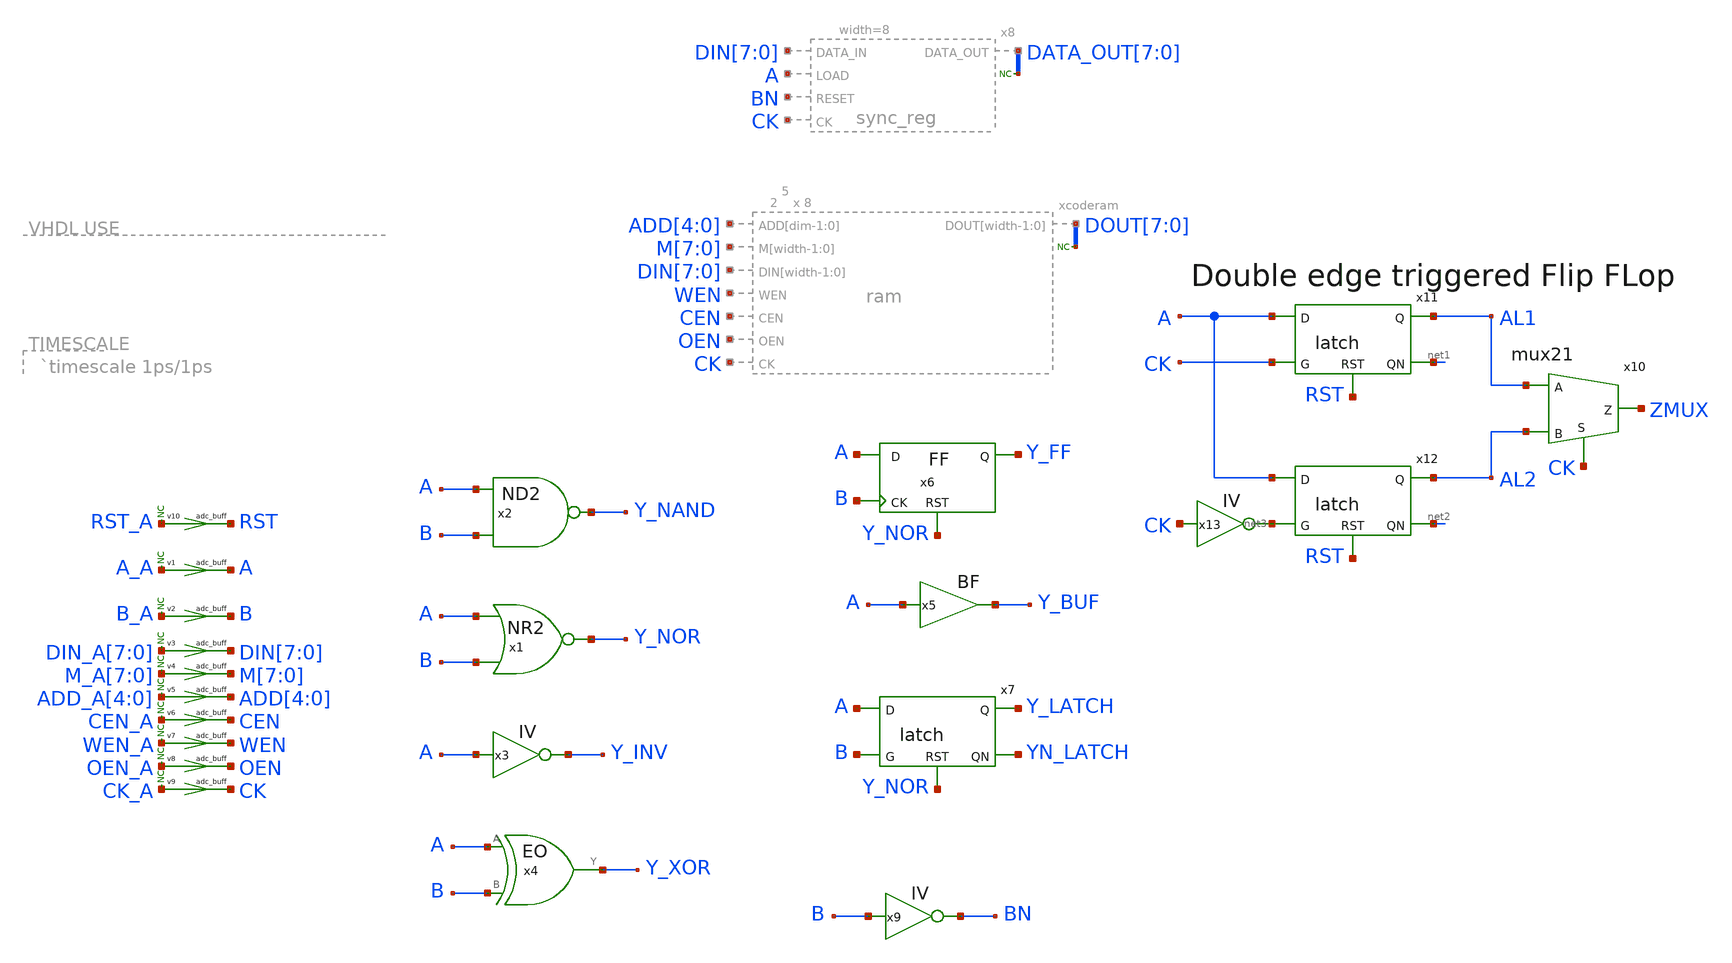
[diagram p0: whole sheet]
** sch_path: xschem_library/logic/testbench.sch
* Copyright (C) 1998-2026 Stefan Frederik Schippers
* This program is free software; you can redistribute it and/or modify
* it under the terms of the GNU General Public License as published by
* the Free Software Foundation; either version 2 of the License, or
* (at your option) any later version.
* This program is distributed in the hope that it will be useful,
* but WITHOUT ANY WARRANTY; without even the implied warranty of
* MERCHANTABILITY or FITNESS FOR A PARTICULAR PURPOSE.  See the
* GNU General Public License for more details.
* You should have received a copy of the GNU General Public License
* along with this program; if not, write to the Free Software
* xschem_library/logic/bf.sym:
* Copyright (C) 1998-2023 Stefan Frederik Schippers
**.subckt testbench
x1 [ A B ] Y_NOR nor
x2 [ A B ] Y_NAND nand
x3 [ A ] Y_INV inv
x4 Y_XOR A B eo
x5 Y_BUF A bf
x6 A Y_FF B Y_NOR ff
x7 A Y_LATCH B Y_NOR YN_LATCH latch
x9 [ B ] BN inv
v1 [ A_A ] [ A ] adc_buff
v2 [ B_A ] [ B ] adc_buff
v3 [ DIN_A[7] ] [ DIN[7] ] adc_buff
v4 [ M_A[7] ] [ M[7] ] adc_buff
v5 [ ADD_A[4] ] [ ADD[4] ] adc_buff
v6 [ CEN_A ] [ CEN ] adc_buff
v7 [ WEN_A ] [ WEN ] adc_buff
v8 [ OEN_A ] [ OEN ] adc_buff
v9 [ CK_A ] [ CK ] adc_buff
x10 AL1 ZMUX AL2 CK mux21
x11 A AL1 CK RST net1 latch
x12 A AL2 net3 RST net2 latch
x13 [ CK ] net3 inv
v10 [ RST_A ] [ RST ] adc_buff
* noconn RST_A
* noconn A_A
* noconn B_A
* noconn DIN_A[7:0]
* noconn M_A[7:0]
* noconn ADD_A[4:0]
* noconn CEN_A
* noconn WEN_A
* noconn OEN_A
* noconn CK_A
* noconn DOUT[7:0]
* noconn DATA_OUT[7:0]
**.ends

* expanding   symbol:  eo.sym # of pins=3
** sym_path: xschem_library/logic/eo.sym
** sch_path: xschem_library/logic/eo.sch
.subckt eo Y A B  delay=220 ps del=220
*.ipin A
*.ipin B
*.opin Y
* noconn Y
* noconn B
* noconn A
.ends


* expanding   symbol:  bf.sym # of pins=2
** sym_path: xschem_library/logic/bf.sym
** sch_path: xschem_library/logic/bf.sch
.subckt bf Y A  delay=90 ps del=90
*.opin Y
*.ipin A
* noconn Y
* noconn A
.ends


* expanding   symbol:  ff.sym # of pins=4
** sym_path: xschem_library/logic/ff.sym
** sch_path: xschem_library/logic/ff.sch
.subckt ff D Q CK RST  delay=400 ps del=400
*.ipin D
*.opin Q
*.ipin CK
*.ipin RST
* noconn Q
* noconn D
* noconn CK
* noconn RST
.ends


* expanding   symbol:  latch.sym # of pins=5
** sym_path: xschem_library/logic/latch.sym
** sch_path: xschem_library/logic/latch.sch
.subckt latch D Q G RST QN  delay=200 ps del=200
*.opin Q
*.ipin G
*.ipin RST
*.opin QN
*.ipin D
.ends


* expanding   symbol:  ram.sym # of pins=8
** sym_path: xschem_library/logic/ram.sym
** sch_path: xschem_library/logic/ram.sch
.subckt ram ADD[dim-1:0] M[width-1:0] DOUT[width-1:0] DIN[width-1:0] WEN CEN OEN CK  dim=5 width=8
+ hex=0
datafile=ram.list modulename=ram access_delay=3000 oe_delay=300
*.opin DOUT[width-1:0]
*.ipin DIN[width-1:0]
*.ipin CK
*.ipin OEN
*.ipin ADD[dim-1:0]
*.ipin WEN
*.ipin CEN
*.ipin M[width-1:0]
* noconn DOUT[width-1:0]
.ends


* expanding   symbol:  sync_reg.sym # of pins=5
** sym_path: xschem_library/logic/sync_reg.sym
** sch_path: xschem_library/logic/sync_reg.sch
.subckt sync_reg DATA_OUT[width-1:0] CK RESET DATA_IN[width-1:0] LOAD  width=8 del=400 delay=400 ps
*.opin DATA_OUT[width-1:0]
*.ipin CK
*.ipin RESET
*.ipin DATA_IN[width-1:0]
*.ipin LOAD
* noconn DATA_OUT[width-1:0]
.ends


* expanding   symbol:  mux21.sym # of pins=4
** sym_path: xschem_library/logic/mux21.sym
** sch_path: xschem_library/logic/mux21.sch
.subckt mux21 A Z B S  delay=200 ps del=200
*.opin Z
*.ipin S
*.ipin A
*.ipin B
* noconn Z
* noconn A
* noconn B
* noconn S
.ends

.end
